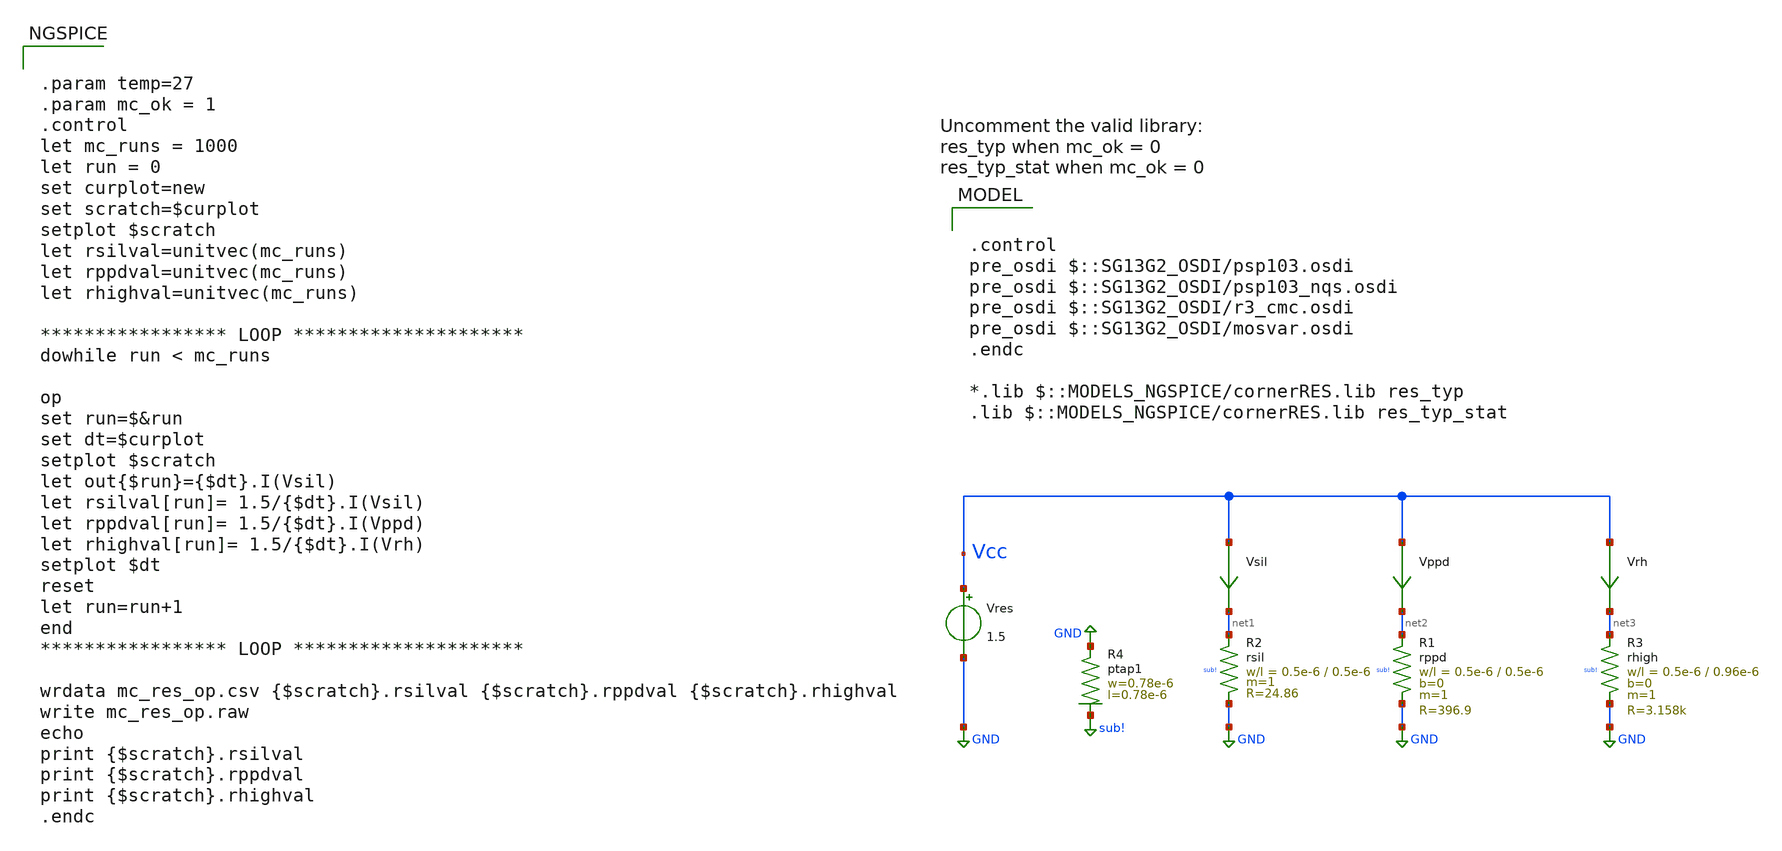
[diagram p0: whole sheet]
** sch_path: ihp-sg13g2/xschem_libs/sg13g2_tests/mc_res_op/schematic/mc_res_op.sch
* Copyright 2023 IHP PDK Authors
**.subckt mc_res_op
Vres Vcc GND 1.5
Vsil Vcc net1 0
.save i(vsil)
Vppd Vcc net2 0
.save i(vppd)
Vrh Vcc net3 0
.save i(vrh)
XR1 net2 GND sub! rppd w=0.5e-6 l=0.5e-6 m=1 b=0 mm_ok=1
XR2 net1 GND sub! rsil w=0.5e-6 l=0.5e-6 m=1 mm_ok=1
XR3 net3 GND sub! rhigh w=0.5e-6 l=0.96e-6 m=1 b=0 mm_ok=1
XR4 GND sub! ptap1 R=262.8 w=0.78e-6 l=0.78e-6
**** begin user architecture code

.control
pre_osdi $::SG13G2_OSDI/psp103.osdi
pre_osdi $::SG13G2_OSDI/psp103_nqs.osdi
pre_osdi $::SG13G2_OSDI/r3_cmc.osdi
pre_osdi $::SG13G2_OSDI/mosvar.osdi
.endc

*.lib $::MODELS_NGSPICE/cornerRES.lib res_typ
.lib $::MODELS_NGSPICE/cornerRES.lib res_typ_stat



.param temp=27
.param mc_ok = 1
.control
let mc_runs = 1000
let run = 0
set curplot=new
set scratch=$curplot
setplot $scratch
let rsilval=unitvec(mc_runs)
let rppdval=unitvec(mc_runs)
let rhighval=unitvec(mc_runs)

***************** LOOP *********************
dowhile run < mc_runs

op
set run=$&run
set dt=$curplot
setplot $scratch
let out{$run}={$dt}.I(Vsil)
let rsilval[run]= 1.5/{$dt}.I(Vsil)
let rppdval[run]= 1.5/{$dt}.I(Vppd)
let rhighval[run]= 1.5/{$dt}.I(Vrh)
setplot $dt
reset
let run=run+1
end
***************** LOOP *********************

wrdata mc_res_op.csv {$scratch}.rsilval {$scratch}.rppdval {$scratch}.rhighval
write mc_res_op.raw
echo
print {$scratch}.rsilval
print {$scratch}.rppdval
print {$scratch}.rhighval
.endc


**** end user architecture code
**.ends
.GLOBAL GND
.GLOBAL sub!
.end
